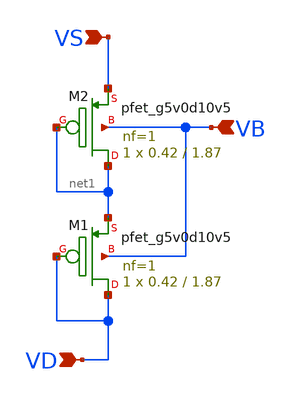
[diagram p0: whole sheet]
** sch_path: pmos/test_bench.sch
**.subckt test_bench VD VS VB
*.ipin VD
*.ipin VS
*.ipin VB
XM2 net1 net1 VS VB sky130_fd_pr__pfet_g5v0d10v5 L=1.87 W=0.42 nf=1 ad='int((1 + 1)/2) * 0.42 / 1 * 0.29'
+ as='int((1 + 2)/2) * 0.42 / 1 * 0.29' pd='2*int((1 + 1)/2) * (0.42 / 1 + 0.29)' ps='2*int((1 + 2)/2) * (0.42 / 1 + 0.29)'
+ nrd='0.29 / 0.42 ' nrs='0.29 / 0.42 ' sa=0 sb=0 sd=0 mult=1 m=1
XM1 VD VD net1 VB sky130_fd_pr__pfet_g5v0d10v5 L=1.87 W=0.42 nf=1 ad='int((1 + 1)/2) * 0.42 / 1 * 0.29'
+ as='int((1 + 2)/2) * 0.42 / 1 * 0.29' pd='2*int((1 + 1)/2) * (0.42 / 1 + 0.29)' ps='2*int((1 + 2)/2) * (0.42 / 1 + 0.29)'
+ nrd='0.29 / 0.42 ' nrs='0.29 / 0.42 ' sa=0 sb=0 sd=0 mult=1 m=1
**.ends
.end
